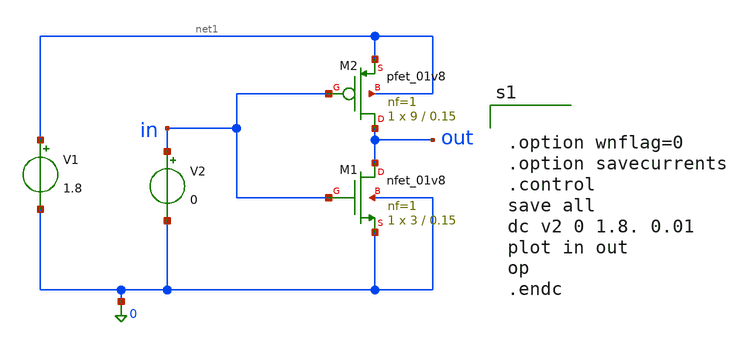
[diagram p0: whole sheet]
** sch_path: CMOS_Inverter_Design.sch
**.subckt CMOS_Inverter_Design
XM1 out in 0 0 sky130_fd_pr__nfet_01v8 L=0.15 W=3 nf=1 ad='int((1 + 1)/2) * 3 / 1 * 0.29' as='int((1 + 2)/2) * 3 / 1 * 0.29'
+ pd='2*int((1 + 1)/2) * (3 / 1 + 0.29)' ps='2*int((1 + 2)/2) * (3 / 1 + 0.29)' nrd='0.29 / 3 ' nrs='0.29 / 3 '
+ sa=0 sb=0 sd=0 mult=1 m=1
V1 net1 0 1.8
V2 in 0 0
XM2 out in net1 net1 sky130_fd_pr__pfet_01v8 L=0.15 W=9 nf=1 ad='int((1 + 1)/2) * 9 / 1 * 0.29' as='int((1 + 2)/2) * 9 / 1 * 0.29'
+ pd='2*int((1 + 1)/2) * (9 / 1 + 0.29)' ps='2*int((1 + 2)/2) * (9 / 1 + 0.29)' nrd='0.29 / 9 ' nrs='0.29 / 9 '
+ sa=0 sb=0 sd=0 mult=1 m=1
**** begin user architecture code



.option wnflag=0
.option savecurrents
.control
save all
dc v2 0 1.8. 0.01
plot in out
op
.endc


**** end user architecture code
**.ends
.end
